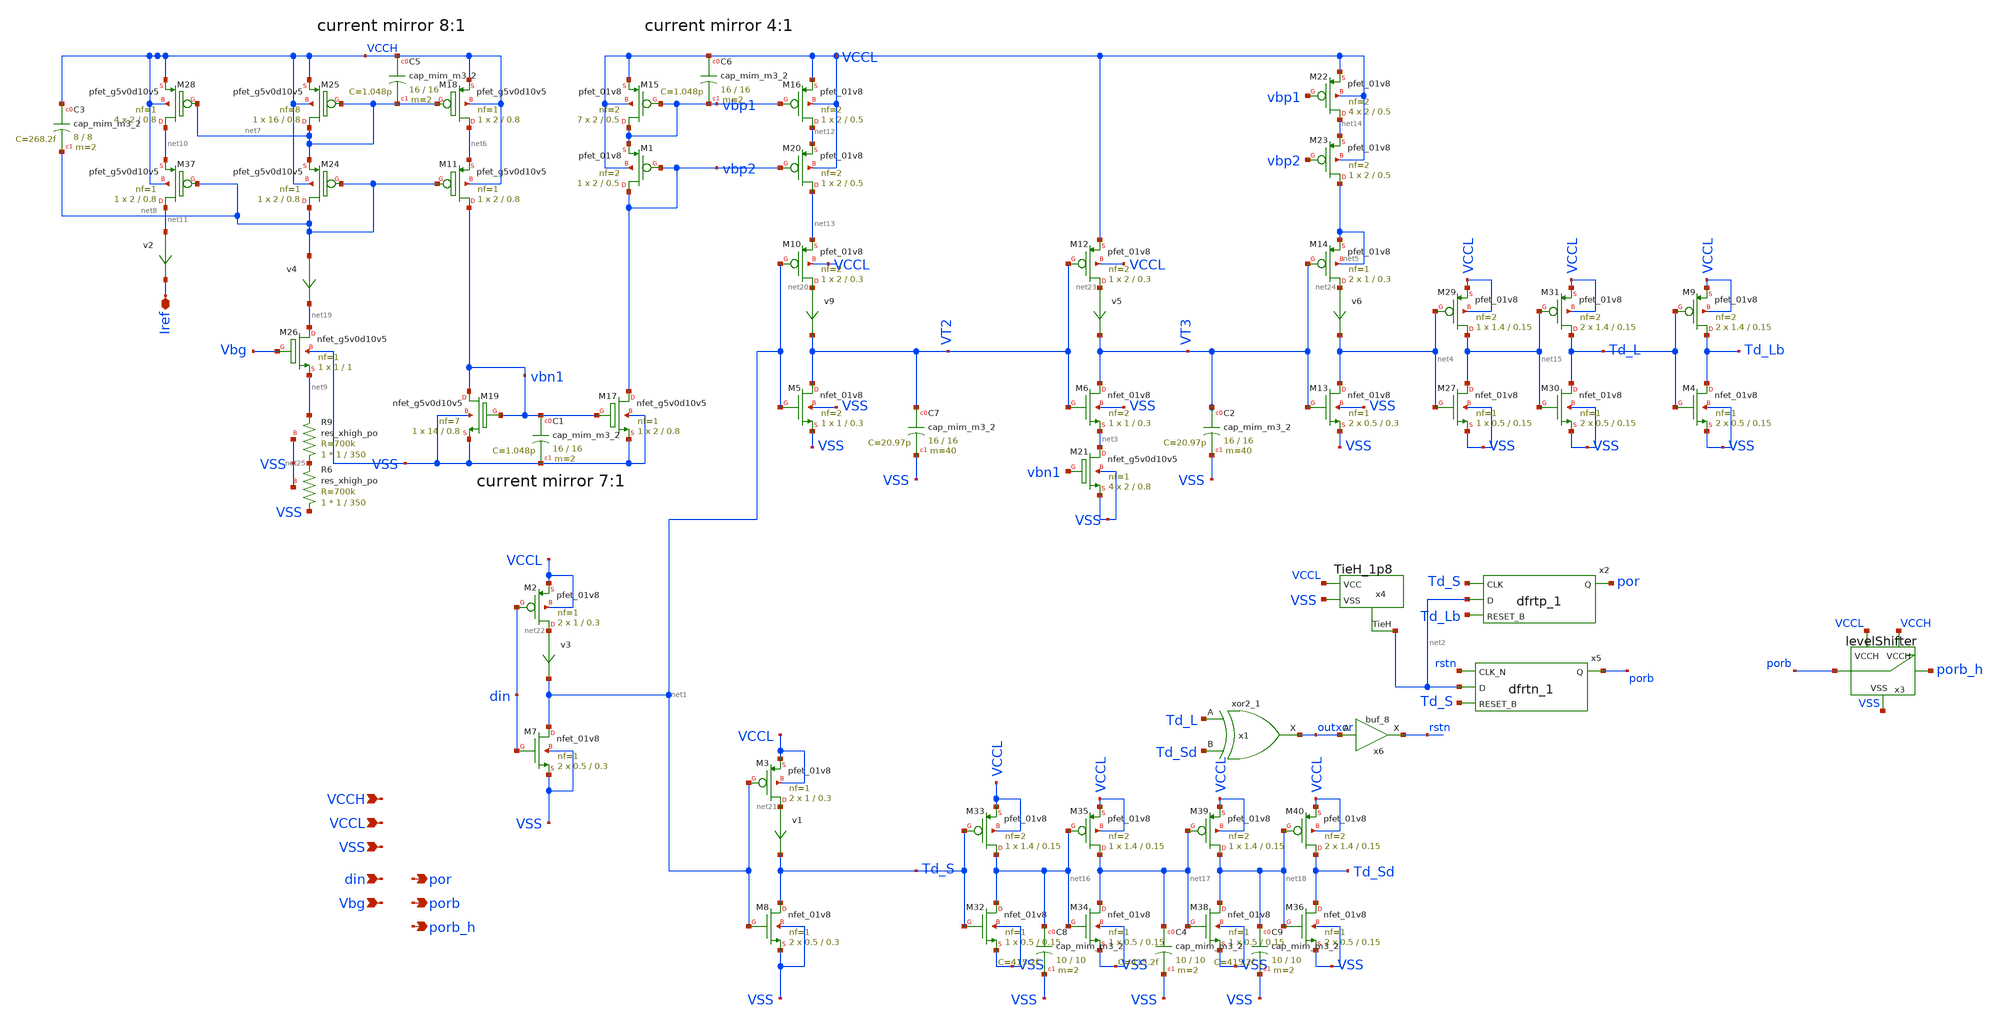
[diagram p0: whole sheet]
** sch_path: xschem_sim/delayPulse_old.sch
**.subckt delayPulse_old VCCL VSS din Vbg por VCCH porb porb_h Iref
*.ipin VCCL
*.ipin VSS
*.ipin din
*.ipin Vbg
*.opin por
*.ipin VCCH
*.opin porb
*.opin porb_h
*.iopin Iref
v9 net20 VT2 0
.save i(v9)
v1 net21 Td_S 0
.save i(v1)
v3 net22 net1 0
.save i(v3)
x1 Td_L Td_Sd VSS VSS VCCL VCCL outxor sky130_fd_sc_hd__xor2_1
x3 porb porb_h VCCL VSS VCCH levelShifter
XM2 net22 din VCCL VCCL sky130_fd_pr__pfet_01v8 L=0.3 W=1 nf=1 ad='int((nf+1)/2) * W/nf * 0.29' as='int((nf+2)/2) * W/nf * 0.29'
+ pd='2*int((nf+1)/2) * (W/nf + 0.29)' ps='2*int((nf+2)/2) * (W/nf + 0.29)' nrd='0.29 / W' nrs='0.29 / W'
+ sa=0 sb=0 sd=0 mult=2 m=2
XM3 net21 net1 VCCL VCCL sky130_fd_pr__pfet_01v8 L=0.3 W=1 nf=1 ad='int((nf+1)/2) * W/nf * 0.29' as='int((nf+2)/2) * W/nf * 0.29'
+ pd='2*int((nf+1)/2) * (W/nf + 0.29)' ps='2*int((nf+2)/2) * (W/nf + 0.29)' nrd='0.29 / W' nrs='0.29 / W'
+ sa=0 sb=0 sd=0 mult=2 m=2
XM5 VT2 net1 VSS VSS sky130_fd_pr__nfet_01v8 L=0.3 W=1 nf=2 ad='int((nf+1)/2) * W/nf * 0.29' as='int((nf+2)/2) * W/nf * 0.29'
+ pd='2*int((nf+1)/2) * (W/nf + 0.29)' ps='2*int((nf+2)/2) * (W/nf + 0.29)' nrd='0.29 / W' nrs='0.29 / W'
+ sa=0 sb=0 sd=0 mult=1 m=1
XM7 net1 din VSS VSS sky130_fd_pr__nfet_01v8 L=0.3 W=0.5 nf=1 ad='int((nf+1)/2) * W/nf * 0.29' as='int((nf+2)/2) * W/nf * 0.29'
+ pd='2*int((nf+1)/2) * (W/nf + 0.29)' ps='2*int((nf+2)/2) * (W/nf + 0.29)' nrd='0.29 / W' nrs='0.29 / W'
+ sa=0 sb=0 sd=0 mult=2 m=2
XM8 Td_S net1 VSS VSS sky130_fd_pr__nfet_01v8 L=0.3 W=0.5 nf=1 ad='int((nf+1)/2) * W/nf * 0.29' as='int((nf+2)/2) * W/nf * 0.29'
+ pd='2*int((nf+1)/2) * (W/nf + 0.29)' ps='2*int((nf+2)/2) * (W/nf + 0.29)' nrd='0.29 / W' nrs='0.29 / W'
+ sa=0 sb=0 sd=0 mult=2 m=2
XM10 net20 net1 net13 VCCL sky130_fd_pr__pfet_01v8 L=0.3 W=2 nf=2 ad='int((nf+1)/2) * W/nf * 0.29' as='int((nf+2)/2) * W/nf * 0.29'
+ pd='2*int((nf+1)/2) * (W/nf + 0.29)' ps='2*int((nf+2)/2) * (W/nf + 0.29)' nrd='0.29 / W' nrs='0.29 / W'
+ sa=0 sb=0 sd=0 mult=1 m=1
v5 net23 VT3 0
.save i(v5)
v6 net24 net4 0
.save i(v6)
XM13 net4 VT3 VSS VSS sky130_fd_pr__nfet_01v8 L=0.3 W=0.5 nf=1 ad='int((nf+1)/2) * W/nf * 0.29' as='int((nf+2)/2) * W/nf * 0.29'
+ pd='2*int((nf+1)/2) * (W/nf + 0.29)' ps='2*int((nf+2)/2) * (W/nf + 0.29)' nrd='0.29 / W' nrs='0.29 / W'
+ sa=0 sb=0 sd=0 mult=2 m=2
XM14 net24 VT3 net5 net5 sky130_fd_pr__pfet_01v8 L=0.3 W=1 nf=1 ad='int((nf+1)/2) * W/nf * 0.29' as='int((nf+2)/2) * W/nf * 0.29'
+ pd='2*int((nf+1)/2) * (W/nf + 0.29)' ps='2*int((nf+2)/2) * (W/nf + 0.29)' nrd='0.29 / W' nrs='0.29 / W'
+ sa=0 sb=0 sd=0 mult=2 m=2
x4 net2 VSS VCCL TieH_1p8
v2 net11 Iref 0
.save i(v2)
XM11 vbn1 net8 net6 VCCH sky130_fd_pr__pfet_g5v0d10v5 L=0.8 W=2 nf=1 ad='int((nf+1)/2) * W/nf * 0.29'
+ as='int((nf+2)/2) * W/nf * 0.29' pd='2*int((nf+1)/2) * (W/nf + 0.29)' ps='2*int((nf+2)/2) * (W/nf + 0.29)'
+ nrd='0.29 / W' nrs='0.29 / W' sa=0 sb=0 sd=0 mult=1 m=1
XM17 vbp2 vbn1 VSS VSS sky130_fd_pr__nfet_g5v0d10v5 L=0.8 W=2 nf=1 ad='int((nf+1)/2) * W/nf * 0.29' as='int((nf+2)/2) * W/nf * 0.29'
+ pd='2*int((nf+1)/2) * (W/nf + 0.29)' ps='2*int((nf+2)/2) * (W/nf + 0.29)' nrd='0.29 / W' nrs='0.29 / W'
+ sa=0 sb=0 sd=0 mult=1 m=1
XM18 net6 net7 VCCH VCCH sky130_fd_pr__pfet_g5v0d10v5 L=0.8 W=2 nf=1 ad='int((nf+1)/2) * W/nf * 0.29'
+ as='int((nf+2)/2) * W/nf * 0.29' pd='2*int((nf+1)/2) * (W/nf + 0.29)' ps='2*int((nf+2)/2) * (W/nf + 0.29)'
+ nrd='0.29 / W' nrs='0.29 / W' sa=0 sb=0 sd=0 mult=1 m=1
XM19 vbn1 vbn1 VSS VSS sky130_fd_pr__nfet_g5v0d10v5 L=0.8 W=14 nf=7 ad='int((nf+1)/2) * W/nf * 0.29'
+ as='int((nf+2)/2) * W/nf * 0.29' pd='2*int((nf+1)/2) * (W/nf + 0.29)' ps='2*int((nf+2)/2) * (W/nf + 0.29)'
+ nrd='0.29 / W' nrs='0.29 / W' sa=0 sb=0 sd=0 mult=1 m=1
XM24 net8 net8 net7 VCCH sky130_fd_pr__pfet_g5v0d10v5 L=0.8 W=2 nf=1 ad='int((nf+1)/2) * W/nf * 0.29'
+ as='int((nf+2)/2) * W/nf * 0.29' pd='2*int((nf+1)/2) * (W/nf + 0.29)' ps='2*int((nf+2)/2) * (W/nf + 0.29)'
+ nrd='0.29 / W' nrs='0.29 / W' sa=0 sb=0 sd=0 mult=1 m=1
XM25 net7 net7 VCCH VCCH sky130_fd_pr__pfet_g5v0d10v5 L=0.8 W=16 nf=8 ad='int((nf+1)/2) * W/nf * 0.29'
+ as='int((nf+2)/2) * W/nf * 0.29' pd='2*int((nf+1)/2) * (W/nf + 0.29)' ps='2*int((nf+2)/2) * (W/nf + 0.29)'
+ nrd='0.29 / W' nrs='0.29 / W' sa=0 sb=0 sd=0 mult=1 m=1
XM26 net19 Vbg net9 VSS sky130_fd_pr__nfet_g5v0d10v5 L=1 W=1 nf=1 ad='int((nf+1)/2) * W/nf * 0.29' as='int((nf+2)/2) * W/nf * 0.29'
+ pd='2*int((nf+1)/2) * (W/nf + 0.29)' ps='2*int((nf+2)/2) * (W/nf + 0.29)' nrd='0.29 / W' nrs='0.29 / W'
+ sa=0 sb=0 sd=0 mult=1 m=1
XM28 net10 net7 VCCH VCCH sky130_fd_pr__pfet_g5v0d10v5 L=0.8 W=2 nf=1 ad='int((nf+1)/2) * W/nf * 0.29'
+ as='int((nf+2)/2) * W/nf * 0.29' pd='2*int((nf+1)/2) * (W/nf + 0.29)' ps='2*int((nf+2)/2) * (W/nf + 0.29)'
+ nrd='0.29 / W' nrs='0.29 / W' sa=0 sb=0 sd=0 mult=4 m=4
XM6 VT3 VT2 net3 VSS sky130_fd_pr__nfet_01v8 L=0.3 W=1 nf=2 ad='int((nf+1)/2) * W/nf * 0.29' as='int((nf+2)/2) * W/nf * 0.29'
+ pd='2*int((nf+1)/2) * (W/nf + 0.29)' ps='2*int((nf+2)/2) * (W/nf + 0.29)' nrd='0.29 / W' nrs='0.29 / W'
+ sa=0 sb=0 sd=0 mult=1 m=1
XM12 net23 VT2 VCCL VCCL sky130_fd_pr__pfet_01v8 L=0.3 W=2 nf=2 ad='int((nf+1)/2) * W/nf * 0.29' as='int((nf+2)/2) * W/nf * 0.29'
+ pd='2*int((nf+1)/2) * (W/nf + 0.29)' ps='2*int((nf+2)/2) * (W/nf + 0.29)' nrd='0.29 / W' nrs='0.29 / W'
+ sa=0 sb=0 sd=0 mult=1 m=1
XM1 vbp2 vbp2 vbp1 VCCL sky130_fd_pr__pfet_01v8 L=0.5 W=2 nf=2 ad='int((nf+1)/2) * W/nf * 0.29' as='int((nf+2)/2) * W/nf * 0.29'
+ pd='2*int((nf+1)/2) * (W/nf + 0.29)' ps='2*int((nf+2)/2) * (W/nf + 0.29)' nrd='0.29 / W' nrs='0.29 / W'
+ sa=0 sb=0 sd=0 mult=1 m=1
XM15 vbp1 vbp1 VCCL VCCL sky130_fd_pr__pfet_01v8 L=0.5 W=2 nf=2 ad='int((nf+1)/2) * W/nf * 0.29' as='int((nf+2)/2) * W/nf * 0.29'
+ pd='2*int((nf+1)/2) * (W/nf + 0.29)' ps='2*int((nf+2)/2) * (W/nf + 0.29)' nrd='0.29 / W' nrs='0.29 / W'
+ sa=0 sb=0 sd=0 mult=7 m=7
XM16 net12 vbp1 VCCL VCCL sky130_fd_pr__pfet_01v8 L=0.5 W=2 nf=2 ad='int((nf+1)/2) * W/nf * 0.29' as='int((nf+2)/2) * W/nf * 0.29'
+ pd='2*int((nf+1)/2) * (W/nf + 0.29)' ps='2*int((nf+2)/2) * (W/nf + 0.29)' nrd='0.29 / W' nrs='0.29 / W'
+ sa=0 sb=0 sd=0 mult=1 m=1
XM20 net13 vbp2 net12 VCCL sky130_fd_pr__pfet_01v8 L=0.5 W=2 nf=2 ad='int((nf+1)/2) * W/nf * 0.29' as='int((nf+2)/2) * W/nf * 0.29'
+ pd='2*int((nf+1)/2) * (W/nf + 0.29)' ps='2*int((nf+2)/2) * (W/nf + 0.29)' nrd='0.29 / W' nrs='0.29 / W'
+ sa=0 sb=0 sd=0 mult=1 m=1
XM21 net3 vbn1 VSS VSS sky130_fd_pr__nfet_g5v0d10v5 L=0.8 W=2 nf=1 ad='int((nf+1)/2) * W/nf * 0.29' as='int((nf+2)/2) * W/nf * 0.29'
+ pd='2*int((nf+1)/2) * (W/nf + 0.29)' ps='2*int((nf+2)/2) * (W/nf + 0.29)' nrd='0.29 / W' nrs='0.29 / W'
+ sa=0 sb=0 sd=0 mult=4 m=4
XM22 net14 vbp1 VCCL VCCL sky130_fd_pr__pfet_01v8 L=0.5 W=2 nf=2 ad='int((nf+1)/2) * W/nf * 0.29' as='int((nf+2)/2) * W/nf * 0.29'
+ pd='2*int((nf+1)/2) * (W/nf + 0.29)' ps='2*int((nf+2)/2) * (W/nf + 0.29)' nrd='0.29 / W' nrs='0.29 / W'
+ sa=0 sb=0 sd=0 mult=4 m=4
XM23 net5 vbp2 net14 VCCL sky130_fd_pr__pfet_01v8 L=0.5 W=2 nf=2 ad='int((nf+1)/2) * W/nf * 0.29' as='int((nf+2)/2) * W/nf * 0.29'
+ pd='2*int((nf+1)/2) * (W/nf + 0.29)' ps='2*int((nf+2)/2) * (W/nf + 0.29)' nrd='0.29 / W' nrs='0.29 / W'
+ sa=0 sb=0 sd=0 mult=1 m=1
XM27 net15 net4 VSS VSS sky130_fd_pr__nfet_01v8 L=0.15 W=0.5 nf=1 ad='int((nf+1)/2) * W/nf * 0.29' as='int((nf+2)/2) * W/nf * 0.29'
+ pd='2*int((nf+1)/2) * (W/nf + 0.29)' ps='2*int((nf+2)/2) * (W/nf + 0.29)' nrd='0.29 / W' nrs='0.29 / W'
+ sa=0 sb=0 sd=0 mult=1 m=1
XM29 net15 net4 VCCL VCCL sky130_fd_pr__pfet_01v8 L=0.15 W=1.4 nf=2 ad='int((nf+1)/2) * W/nf * 0.29'
+ as='int((nf+2)/2) * W/nf * 0.29' pd='2*int((nf+1)/2) * (W/nf + 0.29)' ps='2*int((nf+2)/2) * (W/nf + 0.29)'
+ nrd='0.29 / W' nrs='0.29 / W' sa=0 sb=0 sd=0 mult=1 m=1
XM30 Td_L net15 VSS VSS sky130_fd_pr__nfet_01v8 L=0.15 W=0.5 nf=1 ad='int((nf+1)/2) * W/nf * 0.29' as='int((nf+2)/2) * W/nf * 0.29'
+ pd='2*int((nf+1)/2) * (W/nf + 0.29)' ps='2*int((nf+2)/2) * (W/nf + 0.29)' nrd='0.29 / W' nrs='0.29 / W'
+ sa=0 sb=0 sd=0 mult=2 m=2
XM31 Td_L net15 VCCL VCCL sky130_fd_pr__pfet_01v8 L=0.15 W=1.4 nf=2 ad='int((nf+1)/2) * W/nf * 0.29'
+ as='int((nf+2)/2) * W/nf * 0.29' pd='2*int((nf+1)/2) * (W/nf + 0.29)' ps='2*int((nf+2)/2) * (W/nf + 0.29)'
+ nrd='0.29 / W' nrs='0.29 / W' sa=0 sb=0 sd=0 mult=2 m=2
XM32 net16 Td_S VSS VSS sky130_fd_pr__nfet_01v8 L=0.15 W=0.5 nf=1 ad='int((nf+1)/2) * W/nf * 0.29' as='int((nf+2)/2) * W/nf * 0.29'
+ pd='2*int((nf+1)/2) * (W/nf + 0.29)' ps='2*int((nf+2)/2) * (W/nf + 0.29)' nrd='0.29 / W' nrs='0.29 / W'
+ sa=0 sb=0 sd=0 mult=1 m=1
XM33 net16 Td_S VCCL VCCL sky130_fd_pr__pfet_01v8 L=0.15 W=1.4 nf=2 ad='int((nf+1)/2) * W/nf * 0.29'
+ as='int((nf+2)/2) * W/nf * 0.29' pd='2*int((nf+1)/2) * (W/nf + 0.29)' ps='2*int((nf+2)/2) * (W/nf + 0.29)'
+ nrd='0.29 / W' nrs='0.29 / W' sa=0 sb=0 sd=0 mult=1 m=1
XM34 net17 net16 VSS VSS sky130_fd_pr__nfet_01v8 L=0.15 W=0.5 nf=1 ad='int((nf+1)/2) * W/nf * 0.29' as='int((nf+2)/2) * W/nf * 0.29'
+ pd='2*int((nf+1)/2) * (W/nf + 0.29)' ps='2*int((nf+2)/2) * (W/nf + 0.29)' nrd='0.29 / W' nrs='0.29 / W'
+ sa=0 sb=0 sd=0 mult=1 m=1
XM35 net17 net16 VCCL VCCL sky130_fd_pr__pfet_01v8 L=0.15 W=1.4 nf=2 ad='int((nf+1)/2) * W/nf * 0.29'
+ as='int((nf+2)/2) * W/nf * 0.29' pd='2*int((nf+1)/2) * (W/nf + 0.29)' ps='2*int((nf+2)/2) * (W/nf + 0.29)'
+ nrd='0.29 / W' nrs='0.29 / W' sa=0 sb=0 sd=0 mult=1 m=1
XM36 Td_Sd net18 VSS VSS sky130_fd_pr__nfet_01v8 L=0.15 W=0.5 nf=1 ad='int((nf+1)/2) * W/nf * 0.29' as='int((nf+2)/2) * W/nf * 0.29'
+ pd='2*int((nf+1)/2) * (W/nf + 0.29)' ps='2*int((nf+2)/2) * (W/nf + 0.29)' nrd='0.29 / W' nrs='0.29 / W'
+ sa=0 sb=0 sd=0 mult=2 m=2
XM38 net18 net17 VSS VSS sky130_fd_pr__nfet_01v8 L=0.15 W=0.5 nf=1 ad='int((nf+1)/2) * W/nf * 0.29' as='int((nf+2)/2) * W/nf * 0.29'
+ pd='2*int((nf+1)/2) * (W/nf + 0.29)' ps='2*int((nf+2)/2) * (W/nf + 0.29)' nrd='0.29 / W' nrs='0.29 / W'
+ sa=0 sb=0 sd=0 mult=1 m=1
XM39 net18 net17 VCCL VCCL sky130_fd_pr__pfet_01v8 L=0.15 W=1.4 nf=2 ad='int((nf+1)/2) * W/nf * 0.29'
+ as='int((nf+2)/2) * W/nf * 0.29' pd='2*int((nf+1)/2) * (W/nf + 0.29)' ps='2*int((nf+2)/2) * (W/nf + 0.29)'
+ nrd='0.29 / W' nrs='0.29 / W' sa=0 sb=0 sd=0 mult=1 m=1
x6 outxor VSS VSS VCCL VCCL rstn sky130_fd_sc_hvl__buf_8
XC4 net17 VSS sky130_fd_pr__cap_mim_m3_2 W=10 L=10 MF=2 m=2
XC7 VT2 VSS sky130_fd_pr__cap_mim_m3_2 W=16 L=16 MF=40 m=40
XC2 VT3 VSS sky130_fd_pr__cap_mim_m3_2 W=16 L=16 MF=40 m=40
XC8 net16 VSS sky130_fd_pr__cap_mim_m3_2 W=10 L=10 MF=2 m=2
XC9 net18 VSS sky130_fd_pr__cap_mim_m3_2 W=10 L=10 MF=2 m=2
XM40 Td_Sd net18 VCCL VCCL sky130_fd_pr__pfet_01v8 L=0.15 W=1.4 nf=2 ad='int((nf+1)/2) * W/nf * 0.29'
+ as='int((nf+2)/2) * W/nf * 0.29' pd='2*int((nf+1)/2) * (W/nf + 0.29)' ps='2*int((nf+2)/2) * (W/nf + 0.29)'
+ nrd='0.29 / W' nrs='0.29 / W' sa=0 sb=0 sd=0 mult=2 m=2
XM37 net11 net8 net10 VCCH sky130_fd_pr__pfet_g5v0d10v5 L=0.8 W=2 nf=1 ad='int((nf+1)/2) * W/nf * 0.29'
+ as='int((nf+2)/2) * W/nf * 0.29' pd='2*int((nf+1)/2) * (W/nf + 0.29)' ps='2*int((nf+2)/2) * (W/nf + 0.29)'
+ nrd='0.29 / W' nrs='0.29 / W' sa=0 sb=0 sd=0 mult=1 m=1
v4 net8 net19 0
.save i(v4)
x5 rstn net2 Td_S VSS VSS VCCL VCCL porb sky130_fd_sc_hd__dfrtn_1
x2 Td_S net2 Td_Lb VSS VSS VCCL VCCL por sky130_fd_sc_hd__dfrtp_1
XM4 Td_Lb Td_L VSS VSS sky130_fd_pr__nfet_01v8 L=0.15 W=0.5 nf=1 ad='int((nf+1)/2) * W/nf * 0.29' as='int((nf+2)/2) * W/nf * 0.29'
+ pd='2*int((nf+1)/2) * (W/nf + 0.29)' ps='2*int((nf+2)/2) * (W/nf + 0.29)' nrd='0.29 / W' nrs='0.29 / W'
+ sa=0 sb=0 sd=0 mult=2 m=2
XM9 Td_Lb Td_L VCCL VCCL sky130_fd_pr__pfet_01v8 L=0.15 W=1.4 nf=2 ad='int((nf+1)/2) * W/nf * 0.29' as='int((nf+2)/2) * W/nf * 0.29'
+ pd='2*int((nf+1)/2) * (W/nf + 0.29)' ps='2*int((nf+2)/2) * (W/nf + 0.29)' nrd='0.29 / W' nrs='0.29 / W'
+ sa=0 sb=0 sd=0 mult=2 m=2
XC1 vbn1 VSS sky130_fd_pr__cap_mim_m3_2 W=16 L=16 MF=2 m=2
XC5 VCCH net7 sky130_fd_pr__cap_mim_m3_2 W=16 L=16 MF=2 m=2
XC6 VCCL vbp1 sky130_fd_pr__cap_mim_m3_2 W=16 L=16 MF=2 m=2
XC3 VCCH net8 sky130_fd_pr__cap_mim_m3_2 W=8 L=8 MF=2 m=2
XR9 net25 net9 VSS sky130_fd_pr__res_xhigh_po W=1 L=350 mult=1 m=1
XR6 VSS net25 VSS sky130_fd_pr__res_xhigh_po W=1 L=350 mult=1 m=1
**.ends
.end
